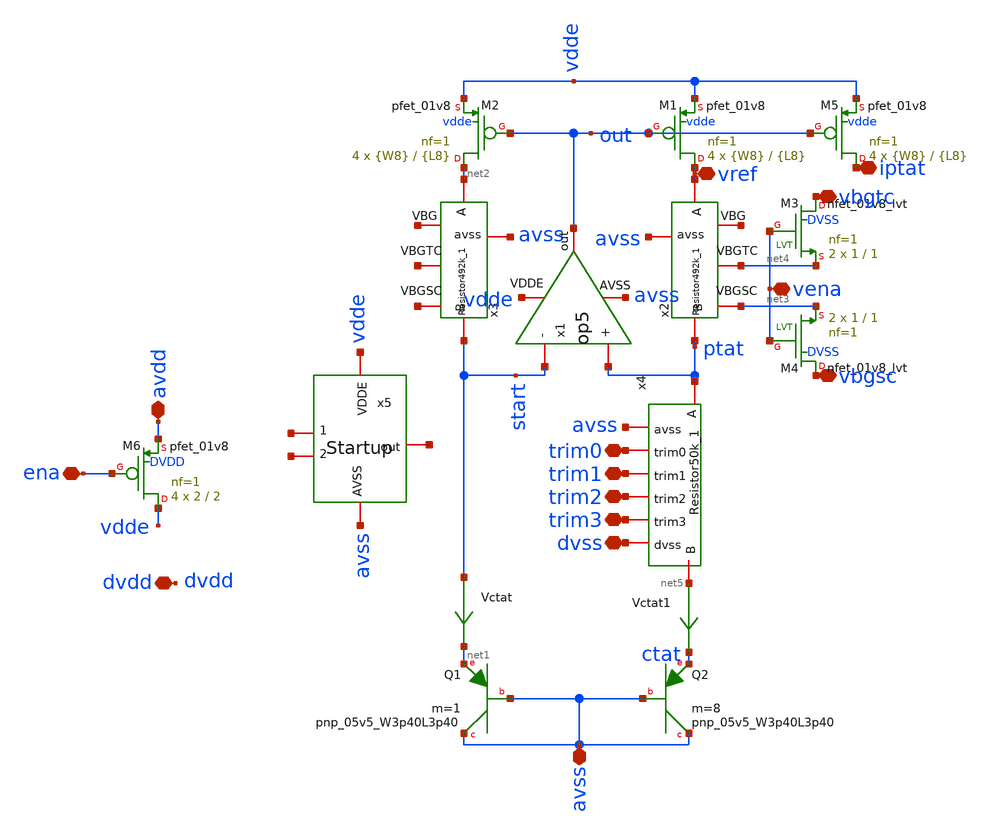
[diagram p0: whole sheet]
** sch_path: xschem/bgr_op5.sch
**.subckt bgr_op5 ena vbgtc vbgsc vena avdd avss dvss trim0 trim1 trim2 trim3 dvdd vref iptat
*.iopin ena
*.iopin vbgtc
*.iopin vbgsc
*.iopin vena
*.iopin avdd
*.iopin avss
*.iopin dvss
*.iopin trim0
*.iopin trim1
*.iopin trim2
*.iopin trim3
*.iopin dvdd
*.iopin vref
*.iopin iptat
XQ1 avss avss net1 sky130_fd_pr__pnp_05v5_W3p40L3p40 m=1
XQ2 avss avss ctat sky130_fd_pr__pnp_05v5_W3p40L3p40 m=8
Vctat start net1 0
.save i(vctat)
XM1 vref out vdde vdde sky130_fd_pr__pfet_01v8 L={L8} W={W8} nf=1 ad='int((nf+1)/2) * W/nf * 0.29' as='int((nf+2)/2) * W/nf * 0.29'
+ pd='2*int((nf+1)/2) * (W/nf + 0.29)' ps='2*int((nf+2)/2) * (W/nf + 0.29)' nrd='0.29 / W' nrs='0.29 / W'
+ sa=0 sb=0 sd=0 mult=4 m=4
XM2 net2 out vdde vdde sky130_fd_pr__pfet_01v8 L={L8} W={W8} nf=1 ad='int((nf+1)/2) * W/nf * 0.29' as='int((nf+2)/2) * W/nf * 0.29'
+ pd='2*int((nf+1)/2) * (W/nf + 0.29)' ps='2*int((nf+2)/2) * (W/nf + 0.29)' nrd='0.29 / W' nrs='0.29 / W'
+ sa=0 sb=0 sd=0 mult=4 m=4
Vctat1 net5 ctat 0
.save i(vctat1)
x2 net6 vref ptat net4 net3 avss Resistor492k_1
x3 net7 net2 start net8 net9 avss Resistor492k_1
x4 avss trim2 trim0 trim1 dvss net5 ptat trim3 Resistor50k_1
x5 vdde net10 net11 net12 avss Startup
XM3 vbgtc vena net4 DVSS sky130_fd_pr__nfet_01v8_lvt L=1 W=1 nf=1 ad='int((nf+1)/2) * W/nf * 0.29' as='int((nf+2)/2) * W/nf * 0.29'
+ pd='2*int((nf+1)/2) * (W/nf + 0.29)' ps='2*int((nf+2)/2) * (W/nf + 0.29)' nrd='0.29 / W' nrs='0.29 / W'
+ sa=0 sb=0 sd=0 mult=2 m=2
XM4 vbgsc vena net3 DVSS sky130_fd_pr__nfet_01v8_lvt L=1 W=1 nf=1 ad='int((nf+1)/2) * W/nf * 0.29' as='int((nf+2)/2) * W/nf * 0.29'
+ pd='2*int((nf+1)/2) * (W/nf + 0.29)' ps='2*int((nf+2)/2) * (W/nf + 0.29)' nrd='0.29 / W' nrs='0.29 / W'
+ sa=0 sb=0 sd=0 mult=2 m=2
XM5 iptat out vdde vdde sky130_fd_pr__pfet_01v8 L={L8} W={W8} nf=1 ad='int((nf+1)/2) * W/nf * 0.29' as='int((nf+2)/2) * W/nf * 0.29'
+ pd='2*int((nf+1)/2) * (W/nf + 0.29)' ps='2*int((nf+2)/2) * (W/nf + 0.29)' nrd='0.29 / W' nrs='0.29 / W'
+ sa=0 sb=0 sd=0 mult=4 m=4
x1 out vdde avss ptat start op5
XM6 vdde ena avdd DVDD sky130_fd_pr__pfet_01v8 L=2 W=2 nf=1 ad='int((nf+1)/2) * W/nf * 0.29' as='int((nf+2)/2) * W/nf * 0.29'
+ pd='2*int((nf+1)/2) * (W/nf + 0.29)' ps='2*int((nf+2)/2) * (W/nf + 0.29)' nrd='0.29 / W' nrs='0.29 / W'
+ sa=0 sb=0 sd=0 mult=4 m=4
**** begin user architecture code


.param L8=10
.param W8=1
.param L10=1
.param W10=1
.param R=492k


**** end user architecture code
**.ends

* expanding   symbol:  Resistor492k_1.sym # of pins=6
** sym_path: xschem/Resistor492k_1.sym
** sch_path: xschem/Resistor492k_1.sch
.subckt Resistor492k_1 VBG A B VBGTC VBGSC avss
*.iopin A
*.iopin VBGTC
*.iopin B
*.iopin VBGSC
*.iopin VBG
*.iopin avss
XR1 net1 A avss sky130_fd_pr__res_high_po_0p35 L={L} mult=1 m=1
XR2 net2 net1 avss sky130_fd_pr__res_high_po_0p35 L={L} mult=1 m=1
XR3 VBG net2 avss sky130_fd_pr__res_high_po_0p35 L={L} mult=1 m=1
XR4 net3 VBG avss sky130_fd_pr__res_high_po_0p35 L={L} mult=1 m=1
XR5 net4 net3 avss sky130_fd_pr__res_high_po_0p35 L={L} mult=1 m=1
**** begin user architecture code


.param L=17


**** end user architecture code
XR6 net5 net6 avss sky130_fd_pr__res_high_po_0p35 L={L} mult=1 m=1
XR7 VBGSC net5 avss sky130_fd_pr__res_high_po_0p35 L={L} mult=1 m=1
XR8 VBGTC VBGSC avss sky130_fd_pr__res_high_po_0p35 L={L} mult=1 m=1
XR9 net7 VBGTC avss sky130_fd_pr__res_high_po_0p35 L={L} mult=1 m=1
XR10 net4 net7 avss sky130_fd_pr__res_high_po_0p35 L={L} mult=1 m=1
XR11 net8 net6 avss sky130_fd_pr__res_high_po_0p35 L={L} mult=1 m=1
XR12 net9 net8 avss sky130_fd_pr__res_high_po_0p35 L={L} mult=1 m=1
XR13 net11 net9 avss sky130_fd_pr__res_high_po_0p35 L={L} mult=1 m=1
XR14 net10 net11 avss sky130_fd_pr__res_high_po_0p35 L={L} mult=1 m=1
XR15 net12 net10 avss sky130_fd_pr__res_high_po_0p35 L={L} mult=1 m=1
XR16 net18 net13 avss sky130_fd_pr__res_high_po_0p35 L={L} mult=1 m=1
XR17 net14 net18 avss sky130_fd_pr__res_high_po_0p35 L={L} mult=1 m=1
XR18 net16 net14 avss sky130_fd_pr__res_high_po_0p35 L={L} mult=1 m=1
XR19 net15 net16 avss sky130_fd_pr__res_high_po_0p35 L={L} mult=1 m=1
XR20 net12 net15 avss sky130_fd_pr__res_high_po_0p35 L={L} mult=1 m=1
XR21 net17 net13 avss sky130_fd_pr__res_high_po_0p35 L={L} mult=1 m=1
XR22 B net17 avss sky130_fd_pr__res_high_po_0p35 L={L} mult=1 m=1
.ends


* expanding   symbol:  Resistor50k_1.sym # of pins=8
** sym_path: xschem/Resistor50k_1.sym
** sch_path: xschem/Resistor50k_1.sch
.subckt Resistor50k_1 avss trim2 trim0 trim1 dvss B A trim3
*.iopin A
*.iopin B
*.iopin avss
*.iopin dvss
*.iopin trim3
*.iopin trim2
*.iopin trim1
*.iopin trim0
XR2 net2 net1 avss sky130_fd_pr__res_high_po_0p35 L={L} mult=1 m=1
**** begin user architecture code


.param L=17
.param La=8.4
.param L1=1
.param W1=4


**** end user architecture code
XR3 A net2 avss sky130_fd_pr__res_high_po_0p35 L={L} mult=1 m=1
XR1 net1 net3 avss sky130_fd_pr__res_high_po_0p35 L={La} mult=2 m=2
XR4 net3 net4 avss sky130_fd_pr__res_high_po_0p35 L={La} mult=4 m=4
XR5 net4 net5 avss sky130_fd_pr__res_high_po_0p35 L={La} mult=8 m=8
XR6 net5 B avss sky130_fd_pr__res_high_po_0p35 L={La} mult=16 m=16
XM4 net1 trim3 net3 DVSS sky130_fd_pr__nfet_01v8_lvt L={L1} W={W1} nf=1 ad='int((nf+1)/2) * W/nf * 0.29'
+ as='int((nf+2)/2) * W/nf * 0.29' pd='2*int((nf+1)/2) * (W/nf + 0.29)' ps='2*int((nf+2)/2) * (W/nf + 0.29)'
+ nrd='0.29 / W' nrs='0.29 / W' sa=0 sb=0 sd=0 mult=4 m=4
XM1 net3 trim2 net4 DVSS sky130_fd_pr__nfet_01v8_lvt L={L1} W={W1} nf=1 ad='int((nf+1)/2) * W/nf * 0.29'
+ as='int((nf+2)/2) * W/nf * 0.29' pd='2*int((nf+1)/2) * (W/nf + 0.29)' ps='2*int((nf+2)/2) * (W/nf + 0.29)'
+ nrd='0.29 / W' nrs='0.29 / W' sa=0 sb=0 sd=0 mult=4 m=4
XM2 net4 trim1 net5 DVSS sky130_fd_pr__nfet_01v8_lvt L={L1} W={W1} nf=1 ad='int((nf+1)/2) * W/nf * 0.29'
+ as='int((nf+2)/2) * W/nf * 0.29' pd='2*int((nf+1)/2) * (W/nf + 0.29)' ps='2*int((nf+2)/2) * (W/nf + 0.29)'
+ nrd='0.29 / W' nrs='0.29 / W' sa=0 sb=0 sd=0 mult=4 m=4
XM3 net5 trim0 B DVSS sky130_fd_pr__nfet_01v8_lvt L={L1} W={W1} nf=1 ad='int((nf+1)/2) * W/nf * 0.29'
+ as='int((nf+2)/2) * W/nf * 0.29' pd='2*int((nf+1)/2) * (W/nf + 0.29)' ps='2*int((nf+2)/2) * (W/nf + 0.29)'
+ nrd='0.29 / W' nrs='0.29 / W' sa=0 sb=0 sd=0 mult=4 m=4
.ends


* expanding   symbol:  Startup.sym # of pins=5
** sym_path: xschem/Startup.sym
** sch_path: xschem/Startup.sch
.subckt Startup VDDE 2 1 out AVSS
*.iopin VDDE
*.iopin AVSS
*.iopin out
*.iopin 1
*.iopin 2
XM1 1 out AVSS AVSS sky130_fd_pr__nfet_01v8 L=1 W=1 nf=1 ad='int((nf+1)/2) * W/nf * 0.29' as='int((nf+2)/2) * W/nf * 0.29'
+ pd='2*int((nf+1)/2) * (W/nf + 0.29)' ps='2*int((nf+2)/2) * (W/nf + 0.29)' nrd='0.29 / W' nrs='0.29 / W'
+ sa=0 sb=0 sd=0 mult=4 m=4
XM2 2 1 VDDE VDDE sky130_fd_pr__pfet_01v8 L=10 W=1 nf=1 ad='int((nf+1)/2) * W/nf * 0.29' as='int((nf+2)/2) * W/nf * 0.29'
+ pd='2*int((nf+1)/2) * (W/nf + 0.29)' ps='2*int((nf+2)/2) * (W/nf + 0.29)' nrd='0.29 / W' nrs='0.29 / W'
+ sa=0 sb=0 sd=0 mult=1 m=1
XM3 1 1 VDDE VDDE sky130_fd_pr__pfet_01v8 L=10 W=1 nf=1 ad='int((nf+1)/2) * W/nf * 0.29' as='int((nf+2)/2) * W/nf * 0.29'
+ pd='2*int((nf+1)/2) * (W/nf + 0.29)' ps='2*int((nf+2)/2) * (W/nf + 0.29)' nrd='0.29 / W' nrs='0.29 / W'
+ sa=0 sb=0 sd=0 mult=1 m=1
XM4 out 2 VDDE VDDE sky130_fd_pr__pfet_01v8 L=10 W=1 nf=1 ad='int((nf+1)/2) * W/nf * 0.29' as='int((nf+2)/2) * W/nf * 0.29'
+ pd='2*int((nf+1)/2) * (W/nf + 0.29)' ps='2*int((nf+2)/2) * (W/nf + 0.29)' nrd='0.29 / W' nrs='0.29 / W'
+ sa=0 sb=0 sd=0 mult=1 m=1
x1 AVSS AVSS 2 ResistorStart
.ends


* expanding   symbol:  op5.sym # of pins=5
** sym_path: xschem/op5.sym
** sch_path: xschem/op5.sch
.subckt op5 out VDDE AVSS + -
*.iopin AVSS
*.iopin -
*.iopin +
*.iopin VDDE
*.iopin out
XM8 net1 net2 VDDE vdde sky130_fd_pr__pfet_01v8 L={L7} W={W7} nf=1 ad='int((nf+1)/2) * W/nf * 0.29' as='int((nf+2)/2) * W/nf * 0.29'
+ pd='2*int((nf+1)/2) * (W/nf + 0.29)' ps='2*int((nf+2)/2) * (W/nf + 0.29)' nrd='0.29 / W' nrs='0.29 / W'
+ sa=0 sb=0 sd=0 mult=2 m=2
XM9 net2 net2 VDDE vdde sky130_fd_pr__pfet_01v8 L={L7} W={W7} nf=1 ad='int((nf+1)/2) * W/nf * 0.29' as='int((nf+2)/2) * W/nf * 0.29'
+ pd='2*int((nf+1)/2) * (W/nf + 0.29)' ps='2*int((nf+2)/2) * (W/nf + 0.29)' nrd='0.29 / W' nrs='0.29 / W'
+ sa=0 sb=0 sd=0 mult=2 m=2
XM5 net3 bias AVSS AVSS sky130_fd_pr__nfet_01v8 L={L6} W={W6} nf=1 ad='int((nf+1)/2) * W/nf * 0.29' as='int((nf+2)/2) * W/nf * 0.29'
+ pd='2*int((nf+1)/2) * (W/nf + 0.29)' ps='2*int((nf+2)/2) * (W/nf + 0.29)' nrd='0.29 / W' nrs='0.29 / W'
+ sa=0 sb=0 sd=0 mult=2 m=2
XM10 out net1 VDDE vdde sky130_fd_pr__pfet_01v8 L={L2} W={W2} nf=1 ad='int((nf+1)/2) * W/nf * 0.29' as='int((nf+2)/2) * W/nf * 0.29'
+ pd='2*int((nf+1)/2) * (W/nf + 0.29)' ps='2*int((nf+2)/2) * (W/nf + 0.29)' nrd='0.29 / W' nrs='0.29 / W'
+ sa=0 sb=0 sd=0 mult=4 m=4
**** begin user architecture code


.include /home/gils/sky130_pdk/share/pdk/sky130A/libs.ref/sky130_fd_pr/spice/sky130_fd_pr__cap_vpp_11p5x11p7_l1m1m2m3_shieldm4.model.spice
**************
*PMOS cms
.param L1=10
.param W1=1

**************
*PMOS current differential
.param L7=10
.param W7=1

**************
*differential Pair
.param L4=13
.param W4=0.9

**************
*NMOS current control
.param L6=20
.param W6=1

**************
*Second Stage
.param L2=10
.param W2=1


**** end user architecture code
XM11 out bias AVSS AVSS sky130_fd_pr__nfet_01v8 L={L6} W={W6} nf=1 ad='int((nf+1)/2) * W/nf * 0.29' as='int((nf+2)/2) * W/nf * 0.29'
+ pd='2*int((nf+1)/2) * (W/nf + 0.29)' ps='2*int((nf+2)/2) * (W/nf + 0.29)' nrd='0.29 / W' nrs='0.29 / W'
+ sa=0 sb=0 sd=0 mult=2 m=2
XM3 net1 + net3 AVSS sky130_fd_pr__nfet_01v8 L={L4} W={W4} nf=1 ad='int((nf+1)/2) * W/nf * 0.29' as='int((nf+2)/2) * W/nf * 0.29'
+ pd='2*int((nf+1)/2) * (W/nf + 0.29)' ps='2*int((nf+2)/2) * (W/nf + 0.29)' nrd='0.29 / W' nrs='0.29 / W'
+ sa=0 sb=0 sd=0 mult=2 m=2
XM1 bias net6 VDDE vdde sky130_fd_pr__pfet_01v8 L={L1} W={W1} nf=1 ad='int((nf+1)/2) * W/nf * 0.29' as='int((nf+2)/2) * W/nf * 0.29'
+ pd='2*int((nf+1)/2) * (W/nf + 0.29)' ps='2*int((nf+2)/2) * (W/nf + 0.29)' nrd='0.29 / W' nrs='0.29 / W'
+ sa=0 sb=0 sd=0 mult=2 m=2
XM2 net6 net6 VDDE vdde sky130_fd_pr__pfet_01v8 L={L1} W={W1} nf=1 ad='int((nf+1)/2) * W/nf * 0.29' as='int((nf+2)/2) * W/nf * 0.29'
+ pd='2*int((nf+1)/2) * (W/nf + 0.29)' ps='2*int((nf+2)/2) * (W/nf + 0.29)' nrd='0.29 / W' nrs='0.29 / W'
+ sa=0 sb=0 sd=0 mult=2 m=2
XM6 net6 bias net7 AVSS sky130_fd_pr__nfet_01v8 L={L6} W={W6} nf=1 ad='int((nf+1)/2) * W/nf * 0.29' as='int((nf+2)/2) * W/nf * 0.29'
+ pd='2*int((nf+1)/2) * (W/nf + 0.29)' ps='2*int((nf+2)/2) * (W/nf + 0.29)' nrd='0.29 / W' nrs='0.29 / W'
+ sa=0 sb=0 sd=0 mult=2 m=2
XM7 bias bias AVSS AVSS sky130_fd_pr__nfet_01v8 L={L6} W={W6} nf=1 ad='int((nf+1)/2) * W/nf * 0.29' as='int((nf+2)/2) * W/nf * 0.29'
+ pd='2*int((nf+1)/2) * (W/nf + 0.29)' ps='2*int((nf+2)/2) * (W/nf + 0.29)' nrd='0.29 / W' nrs='0.29 / W'
+ sa=0 sb=0 sd=0 mult=2 m=2
XR4 net7 net8 AVSS sky130_fd_pr__res_high_po_0p35 L=4.5 mult=2 m=2
XM4 net2 - net3 AVSS sky130_fd_pr__nfet_01v8 L={L4} W={W4} nf=1 ad='int((nf+1)/2) * W/nf * 0.29' as='int((nf+2)/2) * W/nf * 0.29'
+ pd='2*int((nf+1)/2) * (W/nf + 0.29)' ps='2*int((nf+2)/2) * (W/nf + 0.29)' nrd='0.29 / W' nrs='0.29 / W'
+ sa=0 sb=0 sd=0 mult=2 m=2
XR1 net1 net4 AVSS sky130_fd_pr__res_high_po_0p35 L=4.5 mult=2 m=2
XR2 net4 net5 AVSS sky130_fd_pr__res_high_po_0p35 L=4.5 mult=2 m=2
XR9 net8 AVSS AVSS sky130_fd_pr__res_high_po_0p35 L=4.5 mult=2 m=2
XC1 net5 out sky130_fd_pr__cap_mim_m3_1 W=10 L=10 MF=4 m=4
.ends


* expanding   symbol:  ResistorStart.sym # of pins=3
** sym_path: xschem/ResistorStart.sym
** sch_path: xschem/ResistorStart.sch
.subckt ResistorStart AVSS B A
*.iopin A
*.iopin B
*.iopin AVSS
XR1 net1 A AVSS sky130_fd_pr__res_high_po_0p35 L=17 mult=1 m=1
XR2 net2 net1 AVSS sky130_fd_pr__res_high_po_0p35 L={L} mult=1 m=1
XR3 net4 net2 AVSS sky130_fd_pr__res_high_po_0p35 L={L} mult=1 m=1
XR4 net3 net4 AVSS sky130_fd_pr__res_high_po_0p35 L={L} mult=1 m=1
XR5 net5 net3 AVSS sky130_fd_pr__res_high_po_0p35 L={L} mult=1 m=1
**** begin user architecture code


.param L=17


**** end user architecture code
XR6 net6 net7 AVSS sky130_fd_pr__res_high_po_0p35 L={L} mult=1 m=1
XR7 net8 net6 AVSS sky130_fd_pr__res_high_po_0p35 L={L} mult=1 m=1
XR8 net10 net8 AVSS sky130_fd_pr__res_high_po_0p35 L={L} mult=1 m=1
XR9 net9 net10 AVSS sky130_fd_pr__res_high_po_0p35 L={L} mult=1 m=1
XR10 net5 net9 AVSS sky130_fd_pr__res_high_po_0p35 L={L} mult=1 m=1
XR11 net11 net7 AVSS sky130_fd_pr__res_high_po_0p35 L={L} mult=1 m=1
XR12 net12 net11 AVSS sky130_fd_pr__res_high_po_0p35 L={L} mult=1 m=1
XR13 net14 net12 AVSS sky130_fd_pr__res_high_po_0p35 L={L} mult=1 m=1
XR14 net13 net14 AVSS sky130_fd_pr__res_high_po_0p35 L={L} mult=1 m=1
XR15 net15 net13 AVSS sky130_fd_pr__res_high_po_0p35 L={L} mult=1 m=1
XR16 net16 net17 AVSS sky130_fd_pr__res_high_po_0p35 L={L} mult=1 m=1
XR17 net18 net16 AVSS sky130_fd_pr__res_high_po_0p35 L={L} mult=1 m=1
XR18 net20 net18 AVSS sky130_fd_pr__res_high_po_0p35 L={L} mult=1 m=1
XR19 net19 net20 AVSS sky130_fd_pr__res_high_po_0p35 L={L} mult=1 m=1
XR20 net15 net19 AVSS sky130_fd_pr__res_high_po_0p35 L={L} mult=1 m=1
XR21 net21 net17 AVSS sky130_fd_pr__res_high_po_0p35 L={L} mult=1 m=1
XR22 net22 net21 AVSS sky130_fd_pr__res_high_po_0p35 L={L} mult=1 m=1
XR23 net23 net22 AVSS sky130_fd_pr__res_high_po_0p35 L={L} mult=1 m=1
XR24 net24 net23 AVSS sky130_fd_pr__res_high_po_0p35 L={L} mult=1 m=1
XR25 net25 net24 AVSS sky130_fd_pr__res_high_po_0p35 L={L} mult=1 m=1
XR26 net26 B AVSS sky130_fd_pr__res_high_po_0p35 L={L} mult=1 m=1
XR27 net27 net26 AVSS sky130_fd_pr__res_high_po_0p35 L={L} mult=1 m=1
XR28 net28 net27 AVSS sky130_fd_pr__res_high_po_0p35 L={L} mult=1 m=1
XR29 net29 net28 AVSS sky130_fd_pr__res_high_po_0p35 L={L} mult=1 m=1
XR30 net25 net29 AVSS sky130_fd_pr__res_high_po_0p35 L={L} mult=1 m=1
.ends

.end
